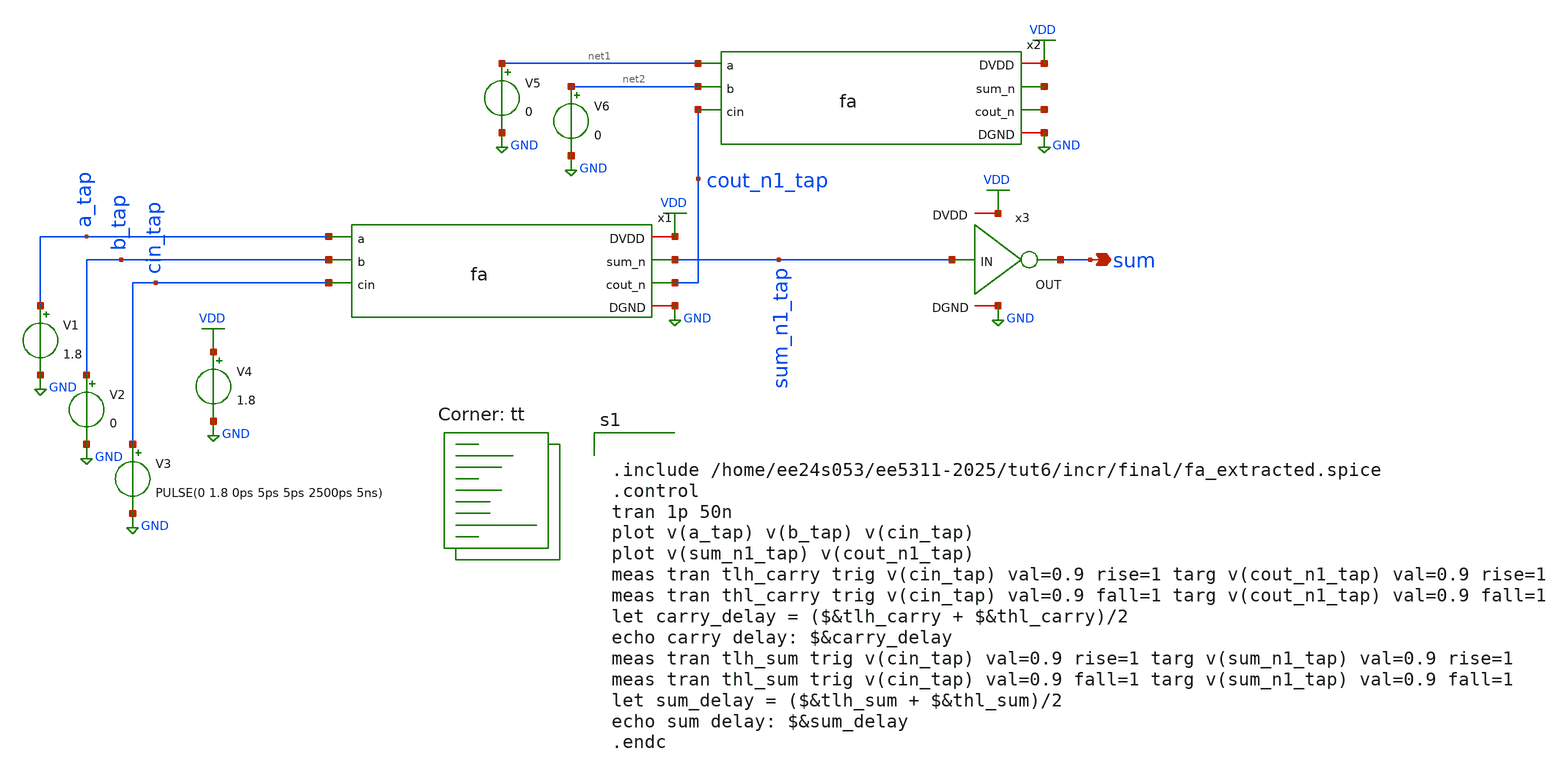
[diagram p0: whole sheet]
** sch_path: tut6/incr/final/fa_tb.sch
**.subckt fa_tb sum
*.opin sum
x1 VDD a_tap b_tap cin_tap sum_n1_tap cout_n1_tap GND fa
x2 VDD net1 net2 cout_n1_tap net3 net4 GND fa
x3 VDD sum sum_n1_tap GND inv
V1 a_tap GND 1.8
V2 b_tap GND 0
V3 cin_tap GND PULSE(0 1.8 0ps 5ps 5ps 2500ps 5ns)
V4 VDD GND 1.8
V5 net1 GND 0
V6 net2 GND 0
**** begin user architecture code


.include /home/ee24s053/ee5311-2025/tut6/incr/final/fa_extracted.spice
.control
tran 1p 50n
plot v(a_tap) v(b_tap) v(cin_tap)
plot v(sum_n1_tap) v(cout_n1_tap)
meas tran tlh_carry trig v(cin_tap) val=0.9 rise=1 targ v(cout_n1_tap) val=0.9 rise=1
meas tran thl_carry trig v(cin_tap) val=0.9 fall=1 targ v(cout_n1_tap) val=0.9 fall=1
let carry_delay = ($&tlh_carry + $&thl_carry)/2
echo carry delay: $&carry_delay
meas tran tlh_sum trig v(cin_tap) val=0.9 rise=1 targ v(sum_n1_tap) val=0.9 rise=1
meas tran thl_sum trig v(cin_tap) val=0.9 fall=1 targ v(sum_n1_tap) val=0.9 fall=1
let sum_delay = ($&tlh_sum + $&thl_sum)/2
echo sum delay: $&sum_delay
.endc


.lib $::SKYWATER_MODELS/sky130.lib.spice tt
**** end user architecture code
**.ends

* expanding   symbol:  /home/ee24s053/ee5311-2025/tut5/inv/cell/subcircuit/inv.sym # of pins=4
** sym_path: tut5/inv/prim/inv.sym
** sch_path: tut5/inv/prim/inv.sch
.subckt inv DVDD OUT IN DGND
*.iopin DVDD
*.iopin DGND
*.opin OUT
*.ipin IN
XM1 OUT IN DVDD DVDD sky130_fd_pr__pfet_01v8 L=0.15 W=0.84 nf=1 ad='int((nf+1)/2) * W/nf * 0.29' as='int((nf+2)/2) * W/nf * 0.29'
+ pd='2*int((nf+1)/2) * (W/nf + 0.29)' ps='2*int((nf+2)/2) * (W/nf + 0.29)' nrd='0.29 / W' nrs='0.29 / W'
+ sa=0 sb=0 sd=0 mult=1 m=1
XM2 OUT IN DGND DGND sky130_fd_pr__nfet_01v8 L=0.15 W=0.42 nf=1 ad='int((nf+1)/2) * W/nf * 0.29' as='int((nf+2)/2) * W/nf * 0.29'
+ pd='2*int((nf+1)/2) * (W/nf + 0.29)' ps='2*int((nf+2)/2) * (W/nf + 0.29)' nrd='0.29 / W' nrs='0.29 / W'
+ sa=0 sb=0 sd=0 mult=1 m=1
.ends

.GLOBAL GND
.GLOBAL VDD
.end
